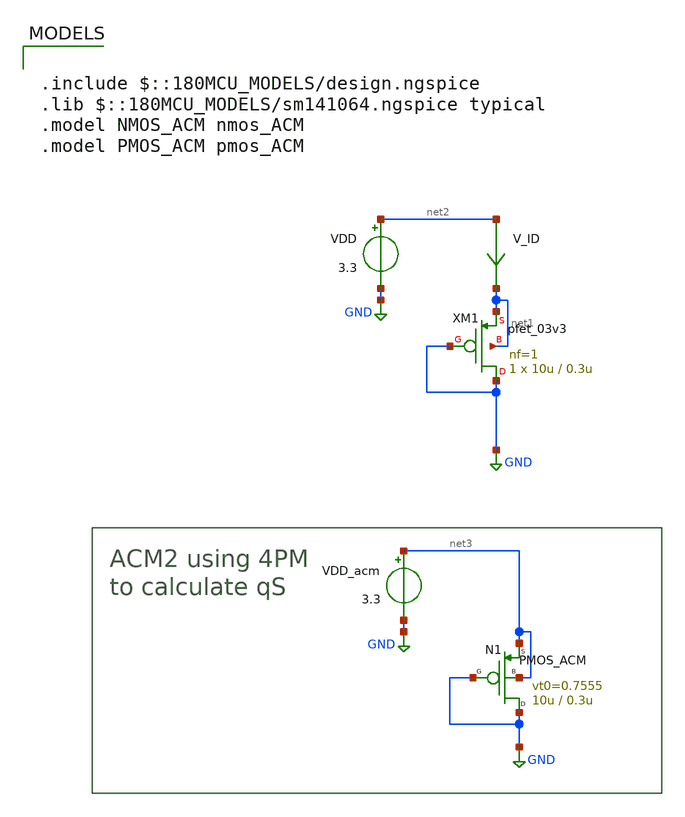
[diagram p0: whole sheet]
** sch_path: legacy/Examples/GF180MCU/xschem/Extraction/pmos_zeta.sch
**.subckt pmos_zeta
VDD net2 GND 3.3
V_ID net2 net1 0
.save i(v_id)
XM1 GND GND net1 net1 pfet_03v3 L=0.3u W=10u nf=1 ad='int((nf+1)/2) * W/nf * 0.18u' as='int((nf+2)/2) * W/nf * 0.18u'
+ pd='2*int((nf+1)/2) * (W/nf + 0.18u)' ps='2*int((nf+2)/2) * (W/nf + 0.18u)' nrd='0.18u / W' nrs='0.18u / W'
+ sa=0 sb=0 sd=0 m=1
VDD_acm net3 GND 3.3
N1 GND GND net3 net3 PMOS_ACM w=10u l=0.3u n=1.43 is=0.709u vt0=0.7555 sigma=18.8m zeta=1p
**** begin user architecture code

.include $::180MCU_MODELS/design.ngspice
.lib $::180MCU_MODELS/sm141064.ngspice typical
.model NMOS_ACM nmos_ACM
.model PMOS_ACM pmos_ACM




.control
pre_osdi ./PMOS_ACM_2V0.osdi
save all

op

let IDsat_=i(V_ID)
save IDsat_

let IS=@n1[is]
save IS

let qS=@n1[qS_op]
save qS

let idsat=IDsat_/IS
save idsat

let sqr=sqrt(1+idsat)
save sqr

let aux1 = 2*(qS+1-sqr)
save aux1

let zeta = aux1/idsat
save zeta

set appenwrite
write pmos_zeta.raw

.endc


**** end user architecture code
**.ends
.GLOBAL GND
.end
